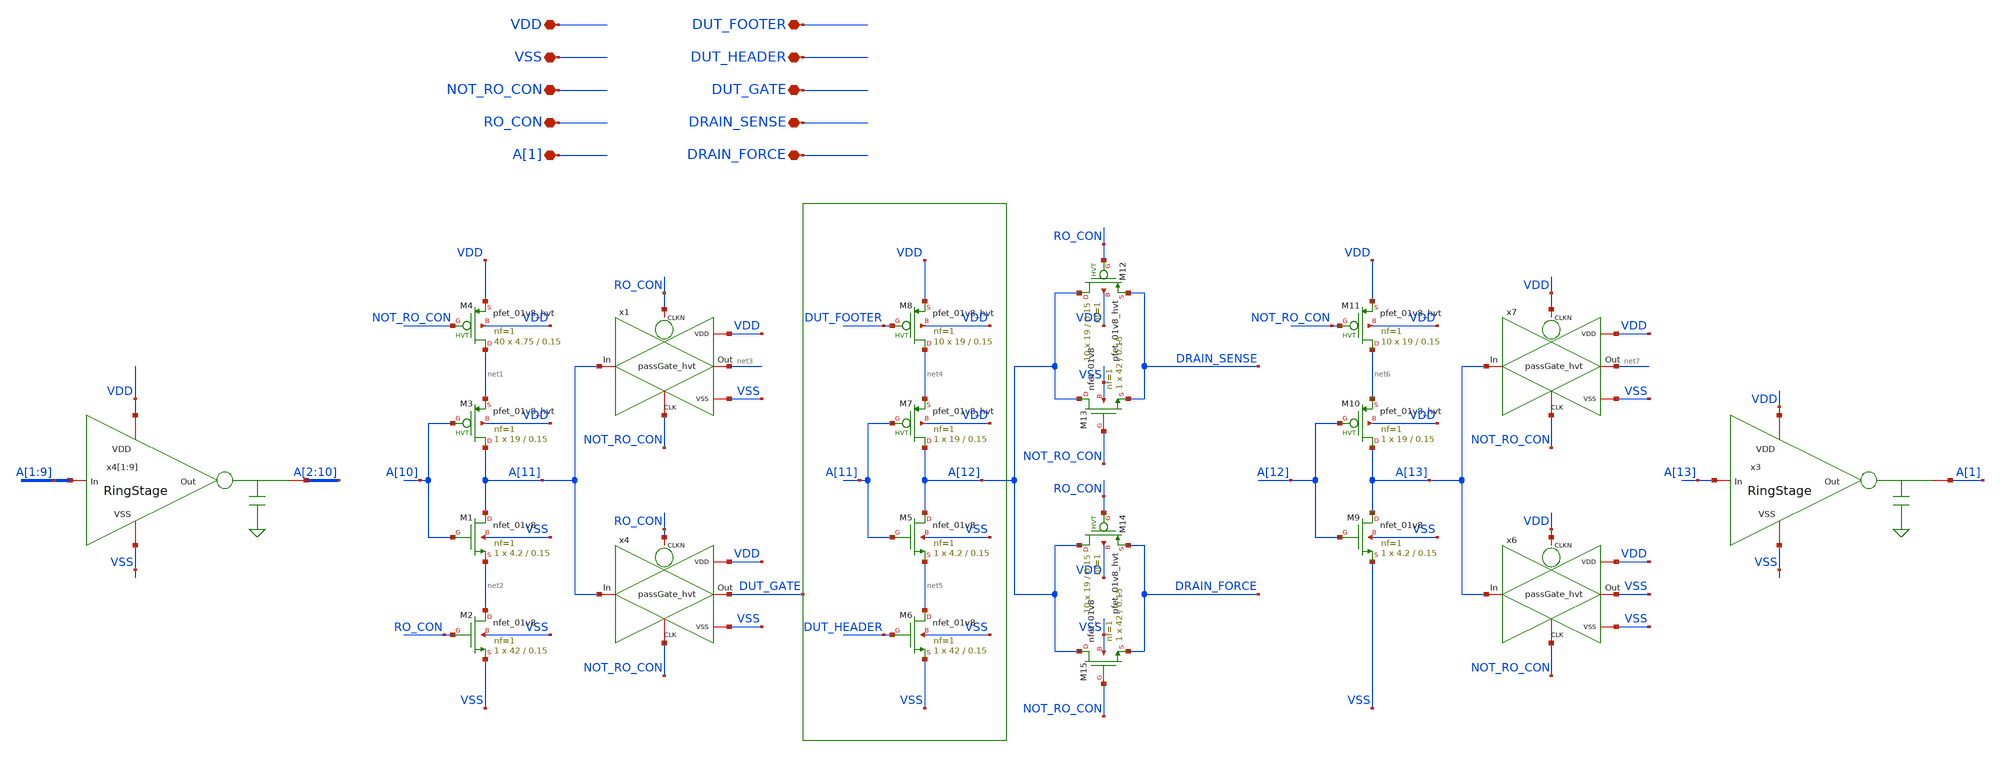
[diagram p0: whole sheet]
** sch_path: HVT/RingOscilator_hvt_13_x10/RingOscilator_hvt_13_x10.sch
**.subckt RingOscilator_hvt_13_x10 VDD VSS NOT_RO_CON RO_CON DUT_FOOTER DUT_HEADER DUT_GATE
*+ DRAIN_SENSE DRAIN_FORCE A[1]
*.iopin VDD
*.iopin VSS
*.iopin NOT_RO_CON
*.iopin RO_CON
*.iopin DUT_FOOTER
*.iopin DUT_HEADER
*.iopin DUT_GATE
*.iopin DRAIN_SENSE
*.iopin DRAIN_FORCE
*.iopin A[1]
XM3 A[11] A[10] net1 VDD sky130_fd_pr__pfet_01v8_hvt L=0.15 W=19 nf=1 ad='int((nf+1)/2) * W/nf * 0.29'
+ as='int((nf+2)/2) * W/nf * 0.29' pd='2*int((nf+1)/2) * (W/nf + 0.29)' ps='2*int((nf+2)/2) * (W/nf + 0.29)'
+ nrd='0.29 / W' nrs='0.29 / W' sa=0 sb=0 sd=0 mult=1 m=1
XM4 net1 NOT_RO_CON VDD VDD sky130_fd_pr__pfet_01v8_hvt L=0.15 W=4.75 nf=1 ad='int((nf+1)/2) * W/nf * 0.29'
+ as='int((nf+2)/2) * W/nf * 0.29' pd='2*int((nf+1)/2) * (W/nf + 0.29)' ps='2*int((nf+2)/2) * (W/nf + 0.29)'
+ nrd='0.29 / W' nrs='0.29 / W' sa=0 sb=0 sd=0 mult=40 m=40
XM7 A[12] A[11] net4 VDD sky130_fd_pr__pfet_01v8_hvt L=0.15 W=19 nf=1 ad='int((nf+1)/2) * W/nf * 0.29'
+ as='int((nf+2)/2) * W/nf * 0.29' pd='2*int((nf+1)/2) * (W/nf + 0.29)' ps='2*int((nf+2)/2) * (W/nf + 0.29)'
+ nrd='0.29 / W' nrs='0.29 / W' sa=0 sb=0 sd=0 mult=1 m=1
XM8 net4 DUT_FOOTER VDD VDD sky130_fd_pr__pfet_01v8_hvt L=0.15 W=19 nf=1 ad='int((nf+1)/2) * W/nf * 0.29'
+ as='int((nf+2)/2) * W/nf * 0.29' pd='2*int((nf+1)/2) * (W/nf + 0.29)' ps='2*int((nf+2)/2) * (W/nf + 0.29)'
+ nrd='0.29 / W' nrs='0.29 / W' sa=0 sb=0 sd=0 mult=10 m=10
XM10 A[13] A[12] net6 VDD sky130_fd_pr__pfet_01v8_hvt L=0.15 W=19 nf=1 ad='int((nf+1)/2) * W/nf * 0.29'
+ as='int((nf+2)/2) * W/nf * 0.29' pd='2*int((nf+1)/2) * (W/nf + 0.29)' ps='2*int((nf+2)/2) * (W/nf + 0.29)'
+ nrd='0.29 / W' nrs='0.29 / W' sa=0 sb=0 sd=0 mult=1 m=1
XM11 net6 NOT_RO_CON VDD VDD sky130_fd_pr__pfet_01v8_hvt L=0.15 W=19 nf=1 ad='int((nf+1)/2) * W/nf * 0.29'
+ as='int((nf+2)/2) * W/nf * 0.29' pd='2*int((nf+1)/2) * (W/nf + 0.29)' ps='2*int((nf+2)/2) * (W/nf + 0.29)'
+ nrd='0.29 / W' nrs='0.29 / W' sa=0 sb=0 sd=0 mult=10 m=10
XM1 A[11] A[10] net2 VSS sky130_fd_pr__nfet_01v8 L=0.15 W=4.2 nf=1 ad='int((nf+1)/2) * W/nf * 0.29' as='int((nf+2)/2) * W/nf * 0.29'
+ pd='2*int((nf+1)/2) * (W/nf + 0.29)' ps='2*int((nf+2)/2) * (W/nf + 0.29)' nrd='0.29 / W' nrs='0.29 / W'
+ sa=0 sb=0 sd=0 mult=1 m=1
XM2 net2 RO_CON VSS VSS sky130_fd_pr__nfet_01v8 L=0.15 W=42 nf=1 ad='int((nf+1)/2) * W/nf * 0.29' as='int((nf+2)/2) * W/nf * 0.29'
+ pd='2*int((nf+1)/2) * (W/nf + 0.29)' ps='2*int((nf+2)/2) * (W/nf + 0.29)' nrd='0.29 / W' nrs='0.29 / W'
+ sa=0 sb=0 sd=0 mult=1 m=1
XM5 A[12] A[11] net5 VSS sky130_fd_pr__nfet_01v8 L=0.15 W=4.2 nf=1 ad='int((nf+1)/2) * W/nf * 0.29' as='int((nf+2)/2) * W/nf * 0.29'
+ pd='2*int((nf+1)/2) * (W/nf + 0.29)' ps='2*int((nf+2)/2) * (W/nf + 0.29)' nrd='0.29 / W' nrs='0.29 / W'
+ sa=0 sb=0 sd=0 mult=1 m=1
XM6 net5 DUT_HEADER VSS VSS sky130_fd_pr__nfet_01v8 L=0.15 W=42 nf=1 ad='int((nf+1)/2) * W/nf * 0.29'
+ as='int((nf+2)/2) * W/nf * 0.29' pd='2*int((nf+1)/2) * (W/nf + 0.29)' ps='2*int((nf+2)/2) * (W/nf + 0.29)'
+ nrd='0.29 / W' nrs='0.29 / W' sa=0 sb=0 sd=0 mult=1 m=1
XM9 A[13] A[12] VSS VSS sky130_fd_pr__nfet_01v8 L=0.15 W=4.2 nf=1 ad='int((nf+1)/2) * W/nf * 0.29' as='int((nf+2)/2) * W/nf * 0.29'
+ pd='2*int((nf+1)/2) * (W/nf + 0.29)' ps='2*int((nf+2)/2) * (W/nf + 0.29)' nrd='0.29 / W' nrs='0.29 / W'
+ sa=0 sb=0 sd=0 mult=1 m=1
x4[1] VDD VSS A[1] A[2] RingStage
x4[2] VDD VSS A[2] A[3] RingStage
x4[3] VDD VSS A[3] A[4] RingStage
x4[4] VDD VSS A[4] A[5] RingStage
x4[5] VDD VSS A[5] A[6] RingStage
x4[6] VDD VSS A[6] A[7] RingStage
x4[7] VDD VSS A[7] A[8] RingStage
x4[8] VDD VSS A[8] A[9] RingStage
x4[9] VDD VSS A[9] A[10] RingStage
x1 A[11] RO_CON VSS VDD NOT_RO_CON net3 passGate_hvt
x4 A[11] RO_CON VSS VDD NOT_RO_CON DUT_GATE passGate_hvt
x6 A[13] VDD VSS VDD NOT_RO_CON VSS passGate_hvt
x7 A[13] VDD VSS VDD NOT_RO_CON net7 passGate_hvt
x3 VDD VSS A[13] A[1] RingStage
XM12 A[12] RO_CON DRAIN_SENSE VDD sky130_fd_pr__pfet_01v8_hvt L=0.15 W=19 nf=1 ad='int((nf+1)/2) * W/nf * 0.29'
+ as='int((nf+2)/2) * W/nf * 0.29' pd='2*int((nf+1)/2) * (W/nf + 0.29)' ps='2*int((nf+2)/2) * (W/nf + 0.29)'
+ nrd='0.29 / W' nrs='0.29 / W' sa=0 sb=0 sd=0 mult=10 m=10
XM13 A[12] NOT_RO_CON DRAIN_SENSE VSS sky130_fd_pr__nfet_01v8 L=0.15 W=42 nf=1 ad='int((nf+1)/2) * W/nf * 0.29'
+ as='int((nf+2)/2) * W/nf * 0.29' pd='2*int((nf+1)/2) * (W/nf + 0.29)' ps='2*int((nf+2)/2) * (W/nf + 0.29)'
+ nrd='0.29 / W' nrs='0.29 / W' sa=0 sb=0 sd=0 mult=1 m=1
XM14 A[12] RO_CON DRAIN_FORCE VDD sky130_fd_pr__pfet_01v8_hvt L=0.15 W=19 nf=1 ad='int((nf+1)/2) * W/nf * 0.29'
+ as='int((nf+2)/2) * W/nf * 0.29' pd='2*int((nf+1)/2) * (W/nf + 0.29)' ps='2*int((nf+2)/2) * (W/nf + 0.29)'
+ nrd='0.29 / W' nrs='0.29 / W' sa=0 sb=0 sd=0 mult=10 m=10
XM15 A[12] NOT_RO_CON DRAIN_FORCE VSS sky130_fd_pr__nfet_01v8 L=0.15 W=42 nf=1 ad='int((nf+1)/2) * W/nf * 0.29'
+ as='int((nf+2)/2) * W/nf * 0.29' pd='2*int((nf+1)/2) * (W/nf + 0.29)' ps='2*int((nf+2)/2) * (W/nf + 0.29)'
+ nrd='0.29 / W' nrs='0.29 / W' sa=0 sb=0 sd=0 mult=1 m=1
**.ends

* expanding   symbol:  /foss/designs/RO_Aging_UNICASS/HVT/RingStage/RingStage.sym # of pins=4
** sym_path: HVT/RingStage/RingStage.sym
** sch_path: HVT/RingStage/RingStage.sch
.subckt RingStage VDD VSS In Out
*.iopin In
*.iopin Out
*.iopin VDD
*.iopin VSS
XM2 Out In VDD VDD sky130_fd_pr__pfet_01v8_hvt L=0.15 W=4.75 nf=1 ad='int((nf+1)/2) * W/nf * 0.29' as='int((nf+2)/2) * W/nf * 0.29'
+ pd='2*int((nf+1)/2) * (W/nf + 0.29)' ps='2*int((nf+2)/2) * (W/nf + 0.29)' nrd='0.29 / W' nrs='0.29 / W'
+ sa=0 sb=0 sd=0 mult=4 m=4
XM1 Out In VSS VSS sky130_fd_pr__nfet_01v8 L=0.15 W=2.1 nf=1 ad='int((nf+1)/2) * W/nf * 0.29' as='int((nf+2)/2) * W/nf * 0.29'
+ pd='2*int((nf+1)/2) * (W/nf + 0.29)' ps='2*int((nf+2)/2) * (W/nf + 0.29)' nrd='0.29 / W' nrs='0.29 / W'
+ sa=0 sb=0 sd=0 mult=2 m=2
XM3 Out VDD net1 VDD sky130_fd_pr__pfet_01v8_hvt L=0.15 W=0.45 nf=1 ad='int((nf+1)/2) * W/nf * 0.29'
+ as='int((nf+2)/2) * W/nf * 0.29' pd='2*int((nf+1)/2) * (W/nf + 0.29)' ps='2*int((nf+2)/2) * (W/nf + 0.29)'
+ nrd='0.29 / W' nrs='0.29 / W' sa=0 sb=0 sd=0 mult=1 m=1
XM4 Out VSS net1 VSS sky130_fd_pr__nfet_01v8 L=0.15 W=0.45 nf=1 ad='int((nf+1)/2) * W/nf * 0.29' as='int((nf+2)/2) * W/nf * 0.29'
+ pd='2*int((nf+1)/2) * (W/nf + 0.29)' ps='2*int((nf+2)/2) * (W/nf + 0.29)' nrd='0.29 / W' nrs='0.29 / W'
+ sa=0 sb=0 sd=0 mult=1 m=1
XM5 Out VDD net2 VDD sky130_fd_pr__pfet_01v8_hvt L=0.15 W=0.45 nf=1 ad='int((nf+1)/2) * W/nf * 0.29'
+ as='int((nf+2)/2) * W/nf * 0.29' pd='2*int((nf+1)/2) * (W/nf + 0.29)' ps='2*int((nf+2)/2) * (W/nf + 0.29)'
+ nrd='0.29 / W' nrs='0.29 / W' sa=0 sb=0 sd=0 mult=1 m=1
XM6 Out VSS net2 VSS sky130_fd_pr__nfet_01v8 L=0.15 W=0.45 nf=1 ad='int((nf+1)/2) * W/nf * 0.29' as='int((nf+2)/2) * W/nf * 0.29'
+ pd='2*int((nf+1)/2) * (W/nf + 0.29)' ps='2*int((nf+2)/2) * (W/nf + 0.29)' nrd='0.29 / W' nrs='0.29 / W'
+ sa=0 sb=0 sd=0 mult=1 m=1
* noconn #net1
* noconn #net2
.ends


* expanding   symbol:  /foss/designs/RO_Aging_UNICASS/HVT/passGate_hvt/passGate_hvt.sym # of pins=6
** sym_path: HVT/passGate_hvt/passGate_hvt.sym
** sch_path: HVT/passGate_hvt/passGate_hvt.sch
.subckt passGate_hvt In CLKN VSS VDD CLK Out
*.iopin In
*.iopin CLKN
*.iopin Out
*.iopin VSS
*.iopin VDD
*.iopin CLK
XM2 Out CLKN In VDD sky130_fd_pr__pfet_01v8_hvt L=0.15 W=0.45 nf=1 ad='int((nf+1)/2) * W/nf * 0.29' as='int((nf+2)/2) * W/nf * 0.29'
+ pd='2*int((nf+1)/2) * (W/nf + 0.29)' ps='2*int((nf+2)/2) * (W/nf + 0.29)' nrd='0.29 / W' nrs='0.29 / W'
+ sa=0 sb=0 sd=0 mult=1 m=1
XM1 Out CLK In VSS sky130_fd_pr__nfet_01v8 L=0.15 W=0.45 nf=1 ad='int((nf+1)/2) * W/nf * 0.29' as='int((nf+2)/2) * W/nf * 0.29'
+ pd='2*int((nf+1)/2) * (W/nf + 0.29)' ps='2*int((nf+2)/2) * (W/nf + 0.29)' nrd='0.29 / W' nrs='0.29 / W'
+ sa=0 sb=0 sd=0 mult=1 m=1
.ends

.end
